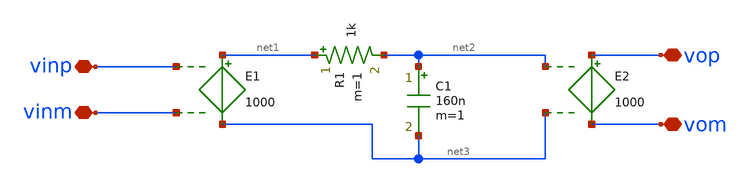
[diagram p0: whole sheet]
** sch_path: xschem/op3.sch
**.subckt op3 vinp vinm vop vom
*.iopin vinp
*.iopin vinm
*.iopin vop
*.iopin vom
E1 net1 net3 vinp vinm 1000
E2 vop vom net2 net3 1000
R1 net1 net2 1k m=1
C1 net2 net3 160n m=1
**.ends
.end
